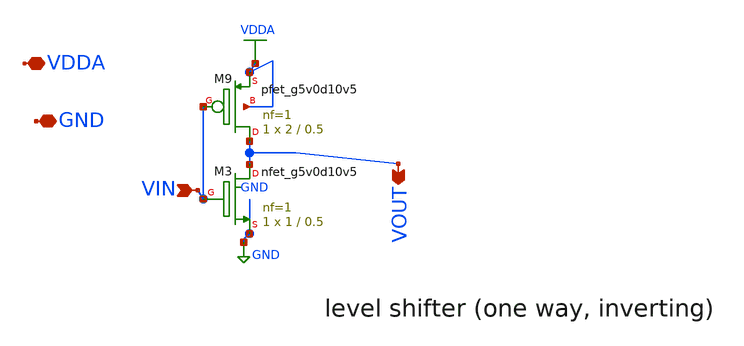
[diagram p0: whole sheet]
** sch_path: xschem/lthinverter.sch
**.subckt lthinverter VOUT GND VIN VDDA
*.opin VOUT
*.iopin GND
*.ipin VIN
*.iopin VDDA
XM9 VOUT VIN VDDA VDDA sky130_fd_pr__pfet_g5v0d10v5 L=0.5 W=2 nf=1 ad='int((1 + 1)/2) * 2 / 1 * 0.29'
+ as='int((1 + 2)/2) * 2 / 1 * 0.29' pd='2*int((1 + 1)/2) * (2 / 1 + 0.29)' ps='2*int((1 + 2)/2) * (2 / 1 + 0.29)'
+ nrd='0.29 / 2 ' nrs='0.29 / 2 ' sa=0 sb=0 sd=0 mult=1 m=1
XM3 VOUT VIN GND GND sky130_fd_pr__nfet_g5v0d10v5 L=0.5 W=1 nf=1 ad='int((nf+1)/2) * W/nf * 0.29' as='int((nf+2)/2) * W/nf * 0.29'
+ pd='2*int((nf+1)/2) * (W/nf + 0.29)' ps='2*int((nf+2)/2) * (W/nf + 0.29)' nrd='0.29 / W' nrs='0.29 / W'
+ sa=0 sb=0 sd=0 mult=1 m=1
**.ends
.GLOBAL GND
.GLOBAL VDDA
.end
